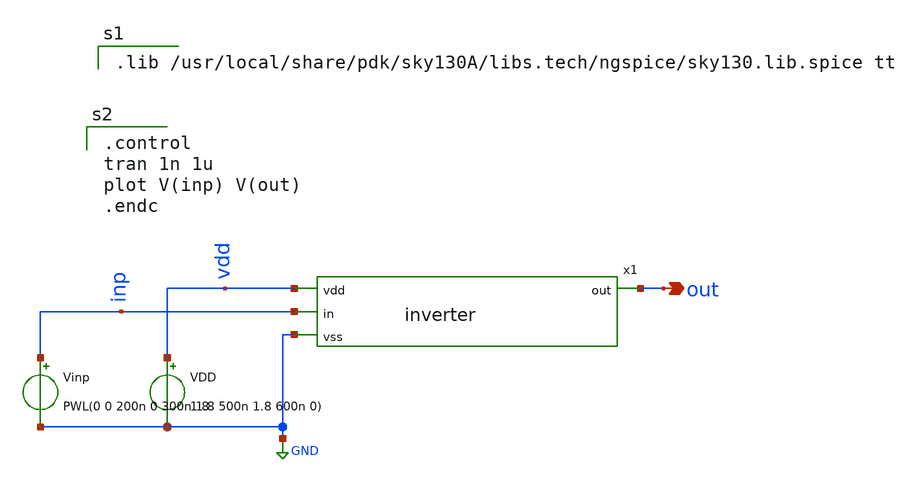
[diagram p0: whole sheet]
** sch_path: xschem/inverter_tb.sch
**.subckt inverter_tb out
*.opin out
x1 vdd inp out GND inverter
VDD vdd GND 1.8
Vinp inp GND PWL(0 0 200n 0 300n 1.8 500n 1.8 600n 0)
**** begin user architecture code

.lib /usr/local/share/pdk/sky130A/libs.tech/ngspice/sky130.lib.spice tt


.control
tran 1n 1u
plot V(inp) V(out)
.endc

**** end user architecture code
**.ends

* expanding   symbol:  inverter.sym # of pins=4
** sym_path: xschem/inverter.sym
** sch_path: xschem/inverter.sch
.subckt inverter vdd in out vss
*.ipin in
*.opin out
*.ipin vdd
*.ipin vss
XM1 out in vss vss sky130_fd_pr__nfet_01v8 L=0.15 W=3 nf=3 ad='int((nf+1)/2) * W/nf * 0.29' as='int((nf+2)/2) * W/nf * 0.29'
+ pd='2*int((nf+1)/2) * (W/nf + 0.29)' ps='2*int((nf+2)/2) * (W/nf + 0.29)' nrd='0.29 / W' nrs='0.29 / W'
+ sa=0 sb=0 sd=0 mult=1 m=1
XM2 out in vdd vdd sky130_fd_pr__pfet_01v8 L=0.15 W=6 nf=3 ad='int((nf+1)/2) * W/nf * 0.29' as='int((nf+2)/2) * W/nf * 0.29'
+ pd='2*int((nf+1)/2) * (W/nf + 0.29)' ps='2*int((nf+2)/2) * (W/nf + 0.29)' nrd='0.29 / W' nrs='0.29 / W'
+ sa=0 sb=0 sd=0 mult=1 m=1
.ends

.GLOBAL GND
.end
